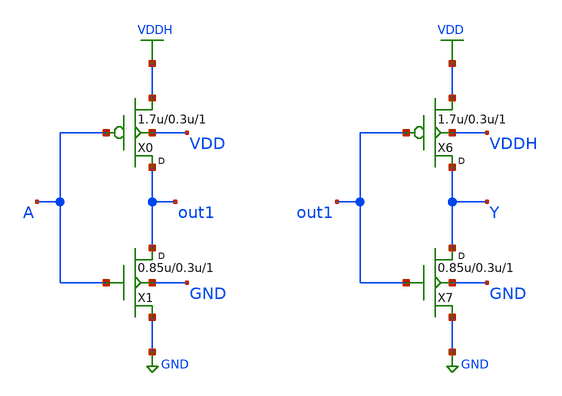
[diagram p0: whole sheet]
** sch_path: lib/12T/lshifdown/gf180mcu_osu_sc_lshifdown.sch
**.subckt gf180mcu_osu_sc_lshifdown
X0 out1 A VDDH VDD pmos_3p3 w=1.7u l=0.3u m=1
X1 out1 A GND GND nmos_3p3 w=0.85u l=0.3u m=1
X6 Y out1 VDD VDDH pmos_3p3 w=1.7u l=0.3u m=1
X7 Y out1 GND GND nmos_3p3 w=0.85u l=0.3u m=1
**.ends
.GLOBAL VDDH
.GLOBAL GND
.GLOBAL VDD
.end
